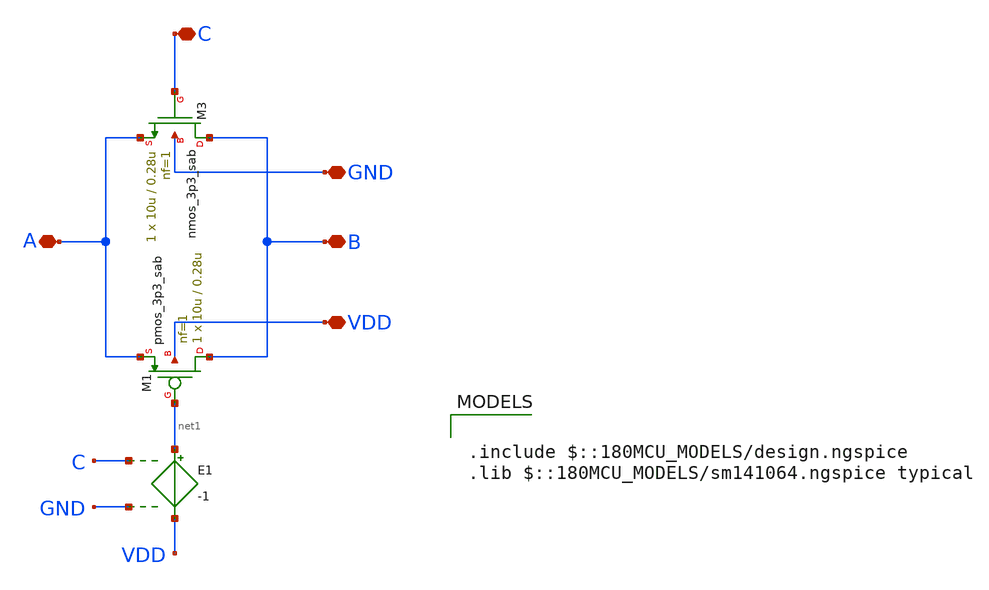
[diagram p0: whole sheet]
** sch_path: Designs/tag_new.sch
**.subckt tag_new B GND A VDD C
*.iopin B
*.iopin GND
*.iopin A
*.iopin VDD
*.iopin C
E1 net1 VDD C GND -1
XM3 B C A GND nmos_3p3_sab L=0.28u W=10u nf=1 ad='int((nf+1)/2) * W/nf * 0.18u' as='int((nf+2)/2) * W/nf * 0.18u'
+ pd='2*int((nf+1)/2) * (W/nf + 0.18u)' ps='2*int((nf+2)/2) * (W/nf + 0.18u)' nrd='0.18u / W' nrs='0.18u / W'
+ sa=0 sb=0 sd=0 m=1
XM1 B net1 A VDD pmos_3p3_sab L=0.28u W=10u nf=1 ad='int((nf+1)/2) * W/nf * 0.18u' as='int((nf+2)/2) * W/nf * 0.18u'
+ pd='2*int((nf+1)/2) * (W/nf + 0.18u)' ps='2*int((nf+2)/2) * (W/nf + 0.18u)' nrd='0.18u / W' nrs='0.18u / W'
+ sa=0 sb=0 sd=0 m=1
**** begin user architecture code

.include $::180MCU_MODELS/design.ngspice
.lib $::180MCU_MODELS/sm141064.ngspice typical

**** end user architecture code
**.ends
.end
